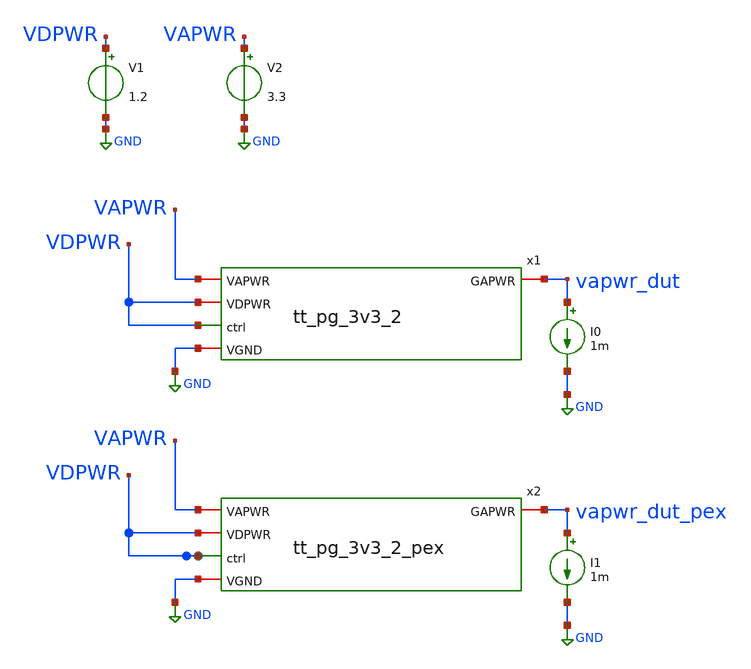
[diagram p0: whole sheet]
** sch_path: pg/ihp-sg13cmos5l/tt_pg_3v3_2/xschem/tb_rdson.sch
**.subckt tb_rdson
x1 GND VDPWR VAPWR vapwr_dut VDPWR tt_pg_3v3_2
I0 vapwr_dut GND 1m
V1 VDPWR GND 1.2
x2 GND VDPWR VAPWR vapwr_dut_pex VDPWR tt_pg_3v3_2_pex
I1 vapwr_dut_pex GND 1m
V2 VAPWR GND 3.3
**** begin user architecture code

.lib cornerMOSlv.lib mos_tt
.lib cornerMOShv.lib mos_tt
.lib cornerCAP.lib cap_typ



.control
save all
dc V2 3.0 3.6 0.05
plot ((v(VAPWR) - v(vapwr_dut)) / 1m) ((v(VAPWR) - v(vapwr_dut_pex)) / 1m)
write tb_rdson.raw
*quit 0
.endc
.end


**** end user architecture code
**.ends
.GLOBAL GND
.end
